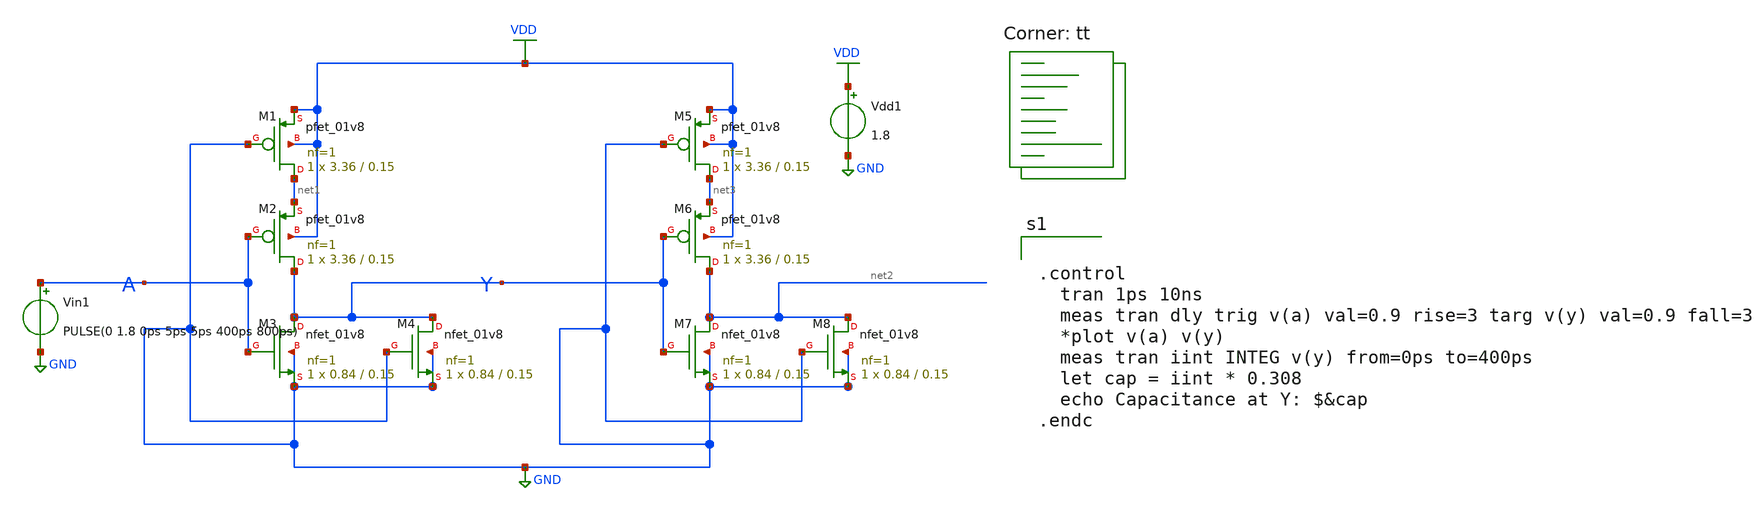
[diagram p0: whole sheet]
** sch_path: lab-exam-midsem/nor2.sch
**.subckt nor2
XM1 net1 GND VDD VDD sky130_fd_pr__pfet_01v8 L=0.15 W=3.36 nf=1 ad='int((nf+1)/2) * W/nf * 0.29' as='int((nf+2)/2) * W/nf * 0.29'
+ pd='2*int((nf+1)/2) * (W/nf + 0.29)' ps='2*int((nf+2)/2) * (W/nf + 0.29)' nrd='0.29 / W' nrs='0.29 / W'
+ sa=0 sb=0 sd=0 mult=1 m=1
XM2 Y A net1 VDD sky130_fd_pr__pfet_01v8 L=0.15 W=3.36 nf=1 ad='int((nf+1)/2) * W/nf * 0.29' as='int((nf+2)/2) * W/nf * 0.29'
+ pd='2*int((nf+1)/2) * (W/nf + 0.29)' ps='2*int((nf+2)/2) * (W/nf + 0.29)' nrd='0.29 / W' nrs='0.29 / W'
+ sa=0 sb=0 sd=0 mult=1 m=1
XM3 Y A GND GND sky130_fd_pr__nfet_01v8 L=0.15 W=0.84 nf=1 ad='int((nf+1)/2) * W/nf * 0.29' as='int((nf+2)/2) * W/nf * 0.29'
+ pd='2*int((nf+1)/2) * (W/nf + 0.29)' ps='2*int((nf+2)/2) * (W/nf + 0.29)' nrd='0.29 / W' nrs='0.29 / W'
+ sa=0 sb=0 sd=0 mult=1 m=1
XM4 Y GND GND GND sky130_fd_pr__nfet_01v8 L=0.15 W=0.84 nf=1 ad='int((nf+1)/2) * W/nf * 0.29' as='int((nf+2)/2) * W/nf * 0.29'
+ pd='2*int((nf+1)/2) * (W/nf + 0.29)' ps='2*int((nf+2)/2) * (W/nf + 0.29)' nrd='0.29 / W' nrs='0.29 / W'
+ sa=0 sb=0 sd=0 mult=1 m=1
XM5 net3 GND VDD VDD sky130_fd_pr__pfet_01v8 L=0.15 W=3.36 nf=1 ad='int((nf+1)/2) * W/nf * 0.29' as='int((nf+2)/2) * W/nf * 0.29'
+ pd='2*int((nf+1)/2) * (W/nf + 0.29)' ps='2*int((nf+2)/2) * (W/nf + 0.29)' nrd='0.29 / W' nrs='0.29 / W'
+ sa=0 sb=0 sd=0 mult=1 m=1
XM6 net2 Y net3 VDD sky130_fd_pr__pfet_01v8 L=0.15 W=3.36 nf=1 ad='int((nf+1)/2) * W/nf * 0.29' as='int((nf+2)/2) * W/nf * 0.29'
+ pd='2*int((nf+1)/2) * (W/nf + 0.29)' ps='2*int((nf+2)/2) * (W/nf + 0.29)' nrd='0.29 / W' nrs='0.29 / W'
+ sa=0 sb=0 sd=0 mult=1 m=1
XM7 net2 Y GND GND sky130_fd_pr__nfet_01v8 L=0.15 W=0.84 nf=1 ad='int((nf+1)/2) * W/nf * 0.29' as='int((nf+2)/2) * W/nf * 0.29'
+ pd='2*int((nf+1)/2) * (W/nf + 0.29)' ps='2*int((nf+2)/2) * (W/nf + 0.29)' nrd='0.29 / W' nrs='0.29 / W'
+ sa=0 sb=0 sd=0 mult=1 m=1
XM8 net2 GND GND GND sky130_fd_pr__nfet_01v8 L=0.15 W=0.84 nf=1 ad='int((nf+1)/2) * W/nf * 0.29' as='int((nf+2)/2) * W/nf * 0.29'
+ pd='2*int((nf+1)/2) * (W/nf + 0.29)' ps='2*int((nf+2)/2) * (W/nf + 0.29)' nrd='0.29 / W' nrs='0.29 / W'
+ sa=0 sb=0 sd=0 mult=1 m=1
Vdd1 VDD GND 1.8
Vin1 A GND PULSE(0 1.8 0ps 5ps 5ps 400ps 800ps)
**** begin user architecture code
.lib $::SKYWATER_MODELS/sky130.lib.spice tt


.control
  tran 1ps 10ns
  meas tran dly trig v(a) val=0.9 rise=3 targ v(y) val=0.9 fall=3
  *plot v(a) v(y)
  meas tran iint INTEG v(y) from=0ps to=400ps
  let cap = iint * 0.308
  echo Capacitance at Y: $&cap
.endc

**** end user architecture code
**.ends
.GLOBAL VDD
.GLOBAL GND
.end
